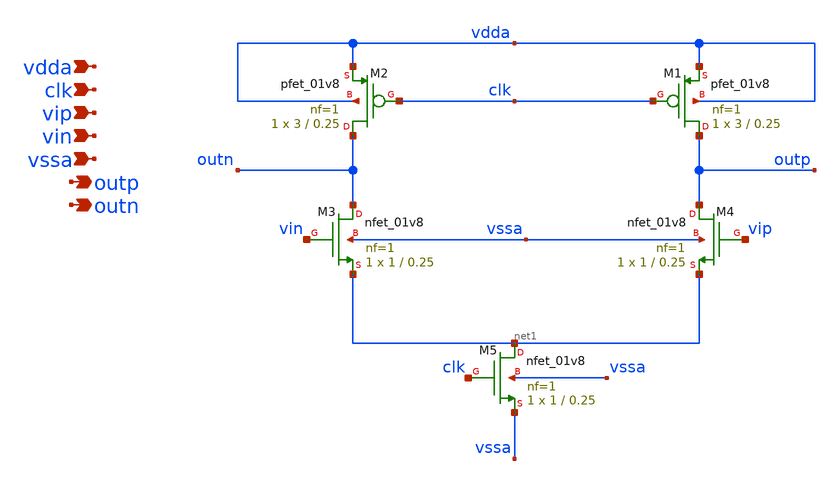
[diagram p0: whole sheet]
** sch_path: xschem/vtc.sch
**.subckt vtc vdda clk vip vin vssa outp outn
*.ipin vdda
*.ipin clk
*.ipin vip
*.ipin vin
*.ipin vssa
*.opin outp
*.opin outn
XM1 outp clk vdda vdda sky130_fd_pr__pfet_01v8 L=0.25 W=3 nf=1 ad='int((nf+1)/2) * W/nf * 0.29' as='int((nf+2)/2) * W/nf * 0.29'
+ pd='2*int((nf+1)/2) * (W/nf + 0.29)' ps='2*int((nf+2)/2) * (W/nf + 0.29)' nrd='0.29 / W' nrs='0.29 / W'
+ sa=0 sb=0 sd=0 mult=1 m=1
XM2 outn clk vdda vdda sky130_fd_pr__pfet_01v8 L=0.25 W=3 nf=1 ad='int((nf+1)/2) * W/nf * 0.29' as='int((nf+2)/2) * W/nf * 0.29'
+ pd='2*int((nf+1)/2) * (W/nf + 0.29)' ps='2*int((nf+2)/2) * (W/nf + 0.29)' nrd='0.29 / W' nrs='0.29 / W'
+ sa=0 sb=0 sd=0 mult=1 m=1
XM3 outn vin net1 vssa sky130_fd_pr__nfet_01v8 L=0.25 W=1 nf=1 ad='int((nf+1)/2) * W/nf * 0.29' as='int((nf+2)/2) * W/nf * 0.29'
+ pd='2*int((nf+1)/2) * (W/nf + 0.29)' ps='2*int((nf+2)/2) * (W/nf + 0.29)' nrd='0.29 / W' nrs='0.29 / W'
+ sa=0 sb=0 sd=0 mult=1 m=1
XM4 outp vip net1 vssa sky130_fd_pr__nfet_01v8 L=0.25 W=1 nf=1 ad='int((nf+1)/2) * W/nf * 0.29' as='int((nf+2)/2) * W/nf * 0.29'
+ pd='2*int((nf+1)/2) * (W/nf + 0.29)' ps='2*int((nf+2)/2) * (W/nf + 0.29)' nrd='0.29 / W' nrs='0.29 / W'
+ sa=0 sb=0 sd=0 mult=1 m=1
XM5 net1 clk vssa vssa sky130_fd_pr__nfet_01v8 L=0.25 W=1 nf=1 ad='int((nf+1)/2) * W/nf * 0.29' as='int((nf+2)/2) * W/nf * 0.29'
+ pd='2*int((nf+1)/2) * (W/nf + 0.29)' ps='2*int((nf+2)/2) * (W/nf + 0.29)' nrd='0.29 / W' nrs='0.29 / W'
+ sa=0 sb=0 sd=0 mult=1 m=1
**.ends
.end
